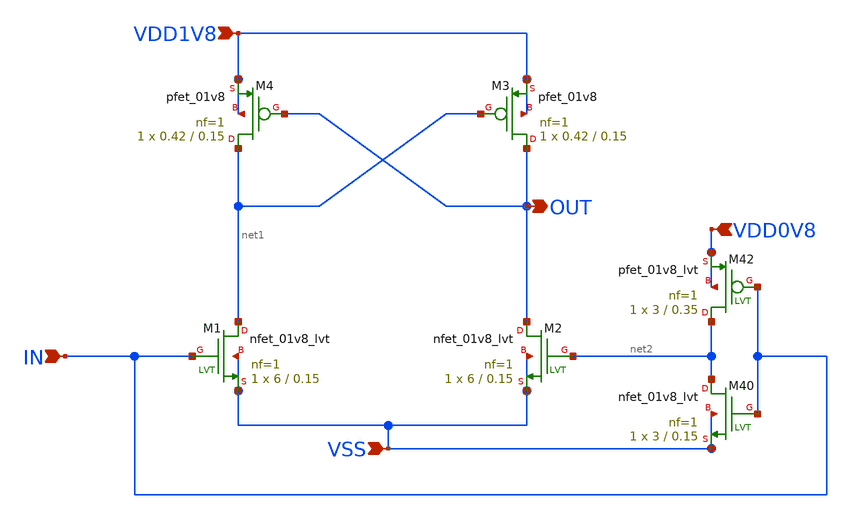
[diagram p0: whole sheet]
** sch_path: design/LELO_SVOD_SKY130A/LELO_SVOD_LEVELSHIFT.sch
**.subckt LELO_SVOD_LEVELSHIFT VDD1V8 VDD0V8 IN VSS OUT
*.ipin VDD1V8
*.ipin VDD0V8
*.ipin IN
*.ipin VSS
*.opin OUT
XM1 net1 IN VSS VSS sky130_fd_pr__nfet_01v8_lvt L=0.15 W=6 nf=1 ad='int((1 + 1)/2) * 6 / 1 * 0.29' as='int((1 + 2)/2) * 6 / 1 * 0.29'
+ pd='2*int((1 + 1)/2) * (6 / 1 + 0.29)' ps='2*int((1 + 2)/2) * (6 / 1 + 0.29)' nrd='0.29 / 6 ' nrs='0.29 / 6 '
+ sa=0 sb=0 sd=0 mult=1 m=1
XM2 OUT net2 VSS VSS sky130_fd_pr__nfet_01v8_lvt L=0.15 W=6 nf=1 ad='int((1 + 1)/2) * 6 / 1 * 0.29' as='int((1 + 2)/2) * 6 / 1 * 0.29'
+ pd='2*int((1 + 1)/2) * (6 / 1 + 0.29)' ps='2*int((1 + 2)/2) * (6 / 1 + 0.29)' nrd='0.29 / 6 ' nrs='0.29 / 6 '
+ sa=0 sb=0 sd=0 mult=1 m=1
XM40 net2 IN VSS VSS sky130_fd_pr__nfet_01v8_lvt L=0.15 W=3 nf=1 ad='int((1 + 1)/2) * 3 / 1 * 0.29' as='int((1 + 2)/2) * 3 / 1 * 0.29'
+ pd='2*int((1 + 1)/2) * (3 / 1 + 0.29)' ps='2*int((1 + 2)/2) * (3 / 1 + 0.29)' nrd='0.29 / 3 ' nrs='0.29 / 3 '
+ sa=0 sb=0 sd=0 mult=1 m=1
XM42 net2 IN VDD0V8 VDD0V8 sky130_fd_pr__pfet_01v8_lvt L=0.35 W=3 nf=1 ad='int((nf+1)/2) * W/nf * 0.29'
+ as='int((nf+2)/2) * W/nf * 0.29' pd='2*int((nf+1)/2) * (W/nf + 0.29)' ps='2*int((nf+2)/2) * (W/nf + 0.29)'
+ nrd='0.29 / W' nrs='0.29 / W' sa=0 sb=0 sd=0 mult=1 m=1
XM3 OUT net1 VDD1V8 VDD1V8 sky130_fd_pr__pfet_01v8 L=0.15 W=0.42 nf=1 ad='int((nf+1)/2) * W/nf * 0.29'
+ as='int((nf+2)/2) * W/nf * 0.29' pd='2*int((nf+1)/2) * (W/nf + 0.29)' ps='2*int((nf+2)/2) * (W/nf + 0.29)'
+ nrd='0.29 / W' nrs='0.29 / W' sa=0 sb=0 sd=0 mult=1 m=1
XM4 net1 OUT VDD1V8 VDD1V8 sky130_fd_pr__pfet_01v8 L=0.15 W=0.42 nf=1 ad='int((nf+1)/2) * W/nf * 0.29'
+ as='int((nf+2)/2) * W/nf * 0.29' pd='2*int((nf+1)/2) * (W/nf + 0.29)' ps='2*int((nf+2)/2) * (W/nf + 0.29)'
+ nrd='0.29 / W' nrs='0.29 / W' sa=0 sb=0 sd=0 mult=1 m=1
**.ends
.end
